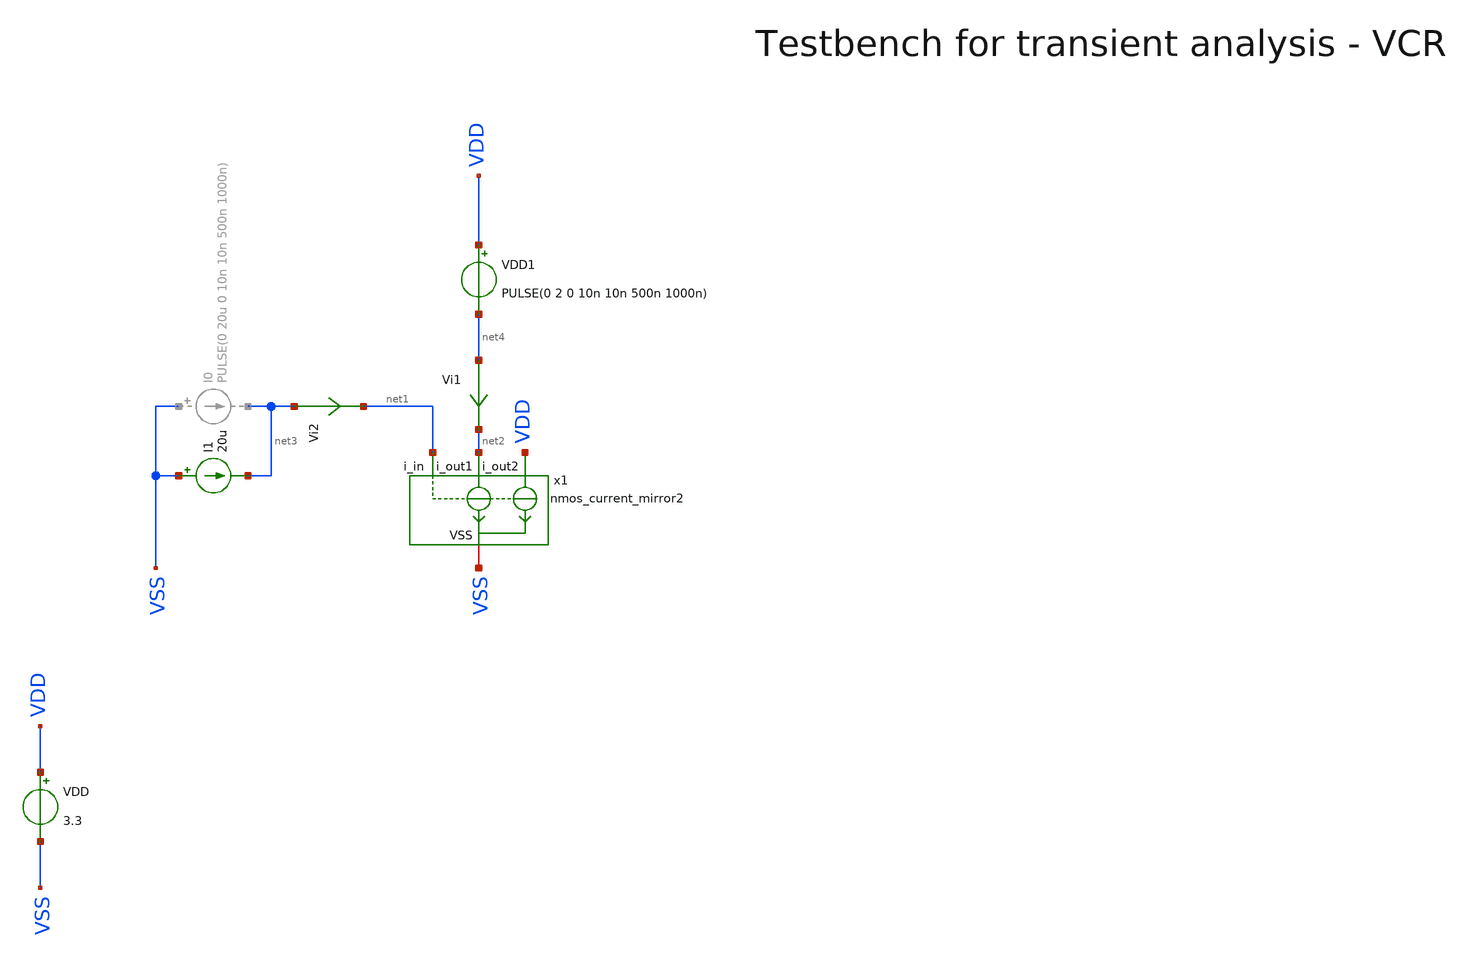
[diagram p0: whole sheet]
** sch_path: macros/heichips26_vcr/macros/switched_capacitor/testbenches/xschem/osc_tb_tran.sch
**.subckt osc_tb_tran
VDD VDD VSS 3.3
x1 net2 net1 VSS VDD nmos_current_mirror2
Vi1 net4 net2 0
.save i(vi1)
Vi2 net3 net1 0
.save i(vi2)
I1 VSS net3 20u
VDD1 VDD net4 PULSE(0 2 0 10n 10n 500n 1000n)
**** begin user architecture code

.lib cornerMOSlv.lib mos_tt
.lib cornerMOShv.lib mos_tt
.lib cornerRES.lib res_typ
.lib cornerDIO.lib dio_tt

.include $::PDK_ROOT/$::PDK/libs.ref/sg13cmos5l_stdcell/spice/sg13cmos5l_stdcell.spice



* .include ../../../netlist/pex/inverter_magic_pex_3.spice
.param VDD=3.3
.csparam VDD=VDD
.param Vcm=VDD/2
.csparam Vcm=Vcm
.param period=60n
.csparam period=period
.param temp=27
.options savecurrents klu method=gear reltol=1e-3 abstol=1e-15 gmin=1e-15
.control

save all
set appendwrite

tran 10n 3000n
remzerovec

save all
set appendwrite

write @schname\.raw
set appendwrite

* Plotting
*plot v(vsweep)
*plot i(Vmeas)
*plot v(sw1)-4 v(sw2)-8
*print mean(v(vd) - v(vb))/mean(i(Vmeas))
plot i(Vi1) i(Vi2)

*quit
.endc


**** end user architecture code
**.ends

* expanding   symbol:  nmos_current_mirror2.sym # of pins=4
** sym_path: macros/heichips26_vcr/macros/switched_capacitor/schematic/xschem/nmos_current_mirror2.sym
** sch_path: macros/heichips26_vcr/macros/switched_capacitor/schematic/xschem/nmos_current_mirror2.sch
.subckt nmos_current_mirror2 i_out1 i_in VSS i_out2
*.ipin i_in
*.opin i_out1
*.iopin VSS
*.opin i_out2
XM1 i_out1 i_in VSS VSS sg13_hv_nmos w=5.0u l=5.0u ng=1 m=1 mm_ok=1
XM2 i_in i_in VSS VSS sg13_hv_nmos w=5.0u l=5.0u ng=1 m=1 mm_ok=1
XM3 i_out2 i_in VSS VSS sg13_hv_nmos w=20.0u l=5.0u ng=5 m=1 mm_ok=1
.ends

.end
